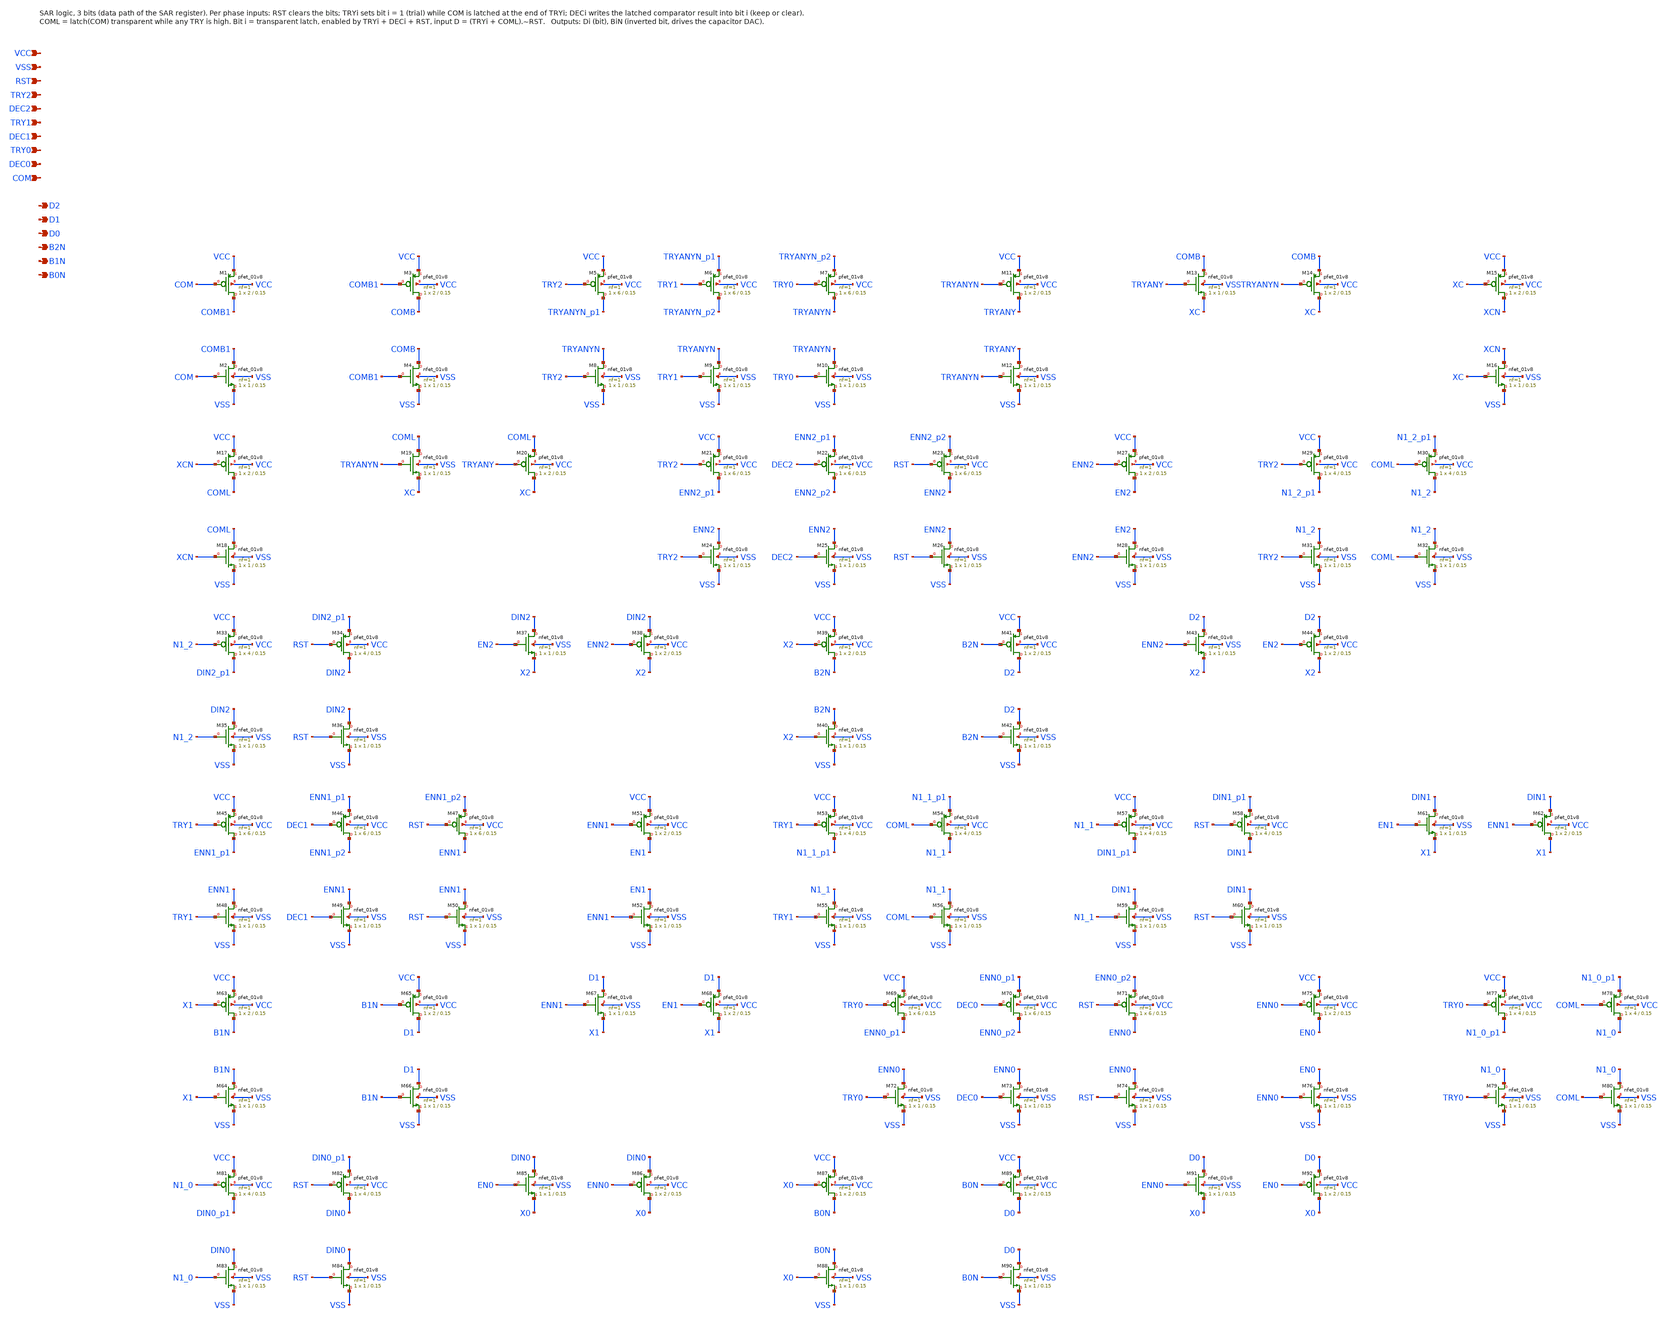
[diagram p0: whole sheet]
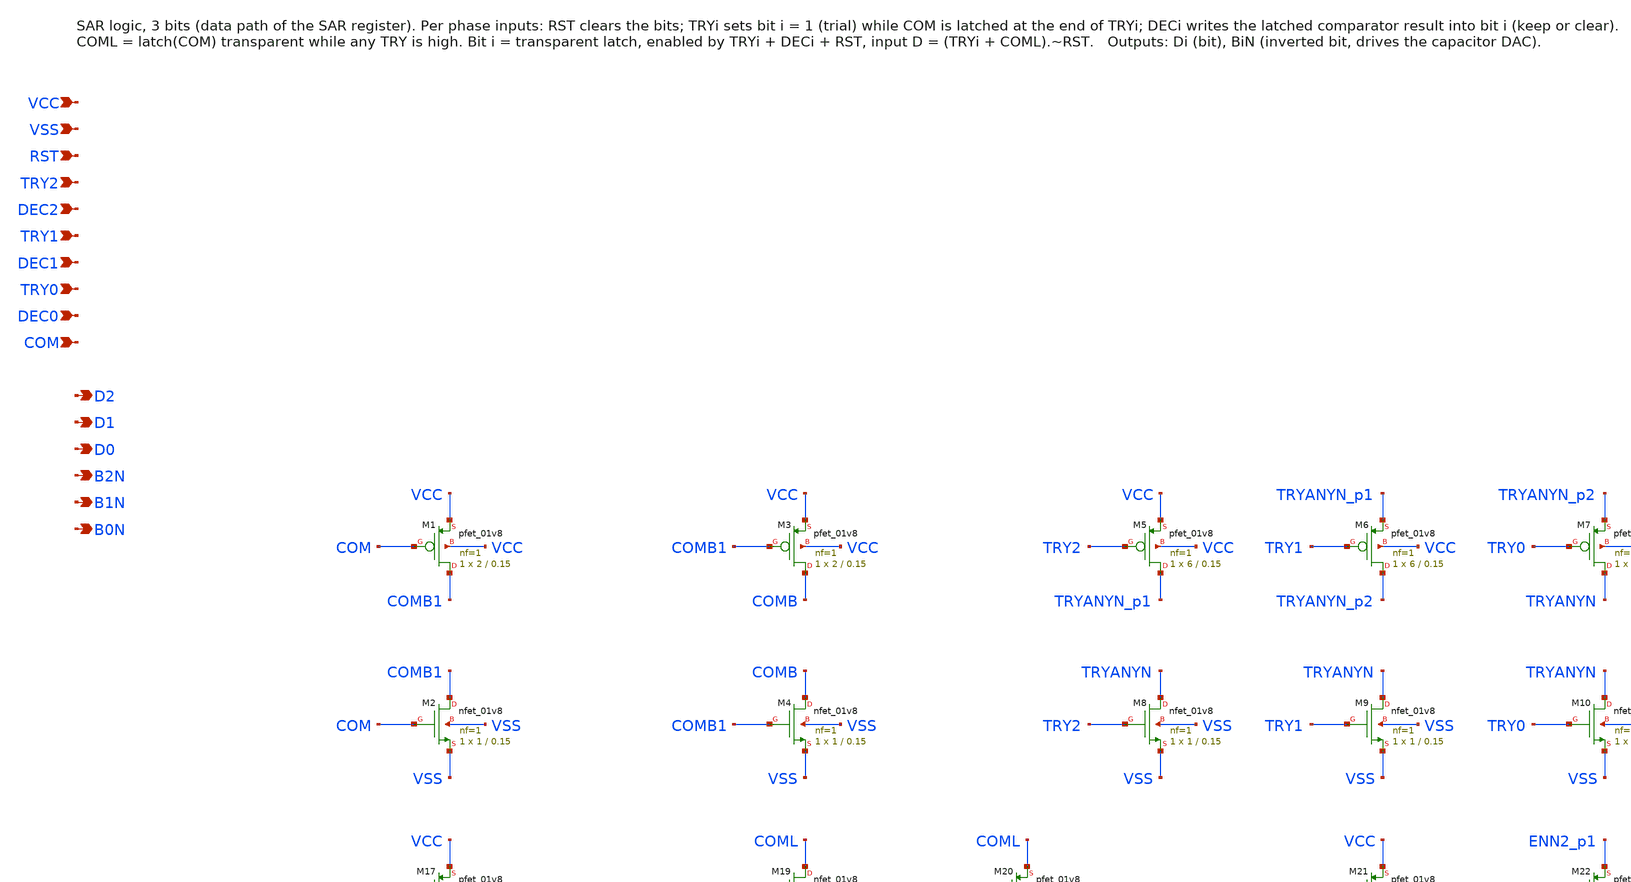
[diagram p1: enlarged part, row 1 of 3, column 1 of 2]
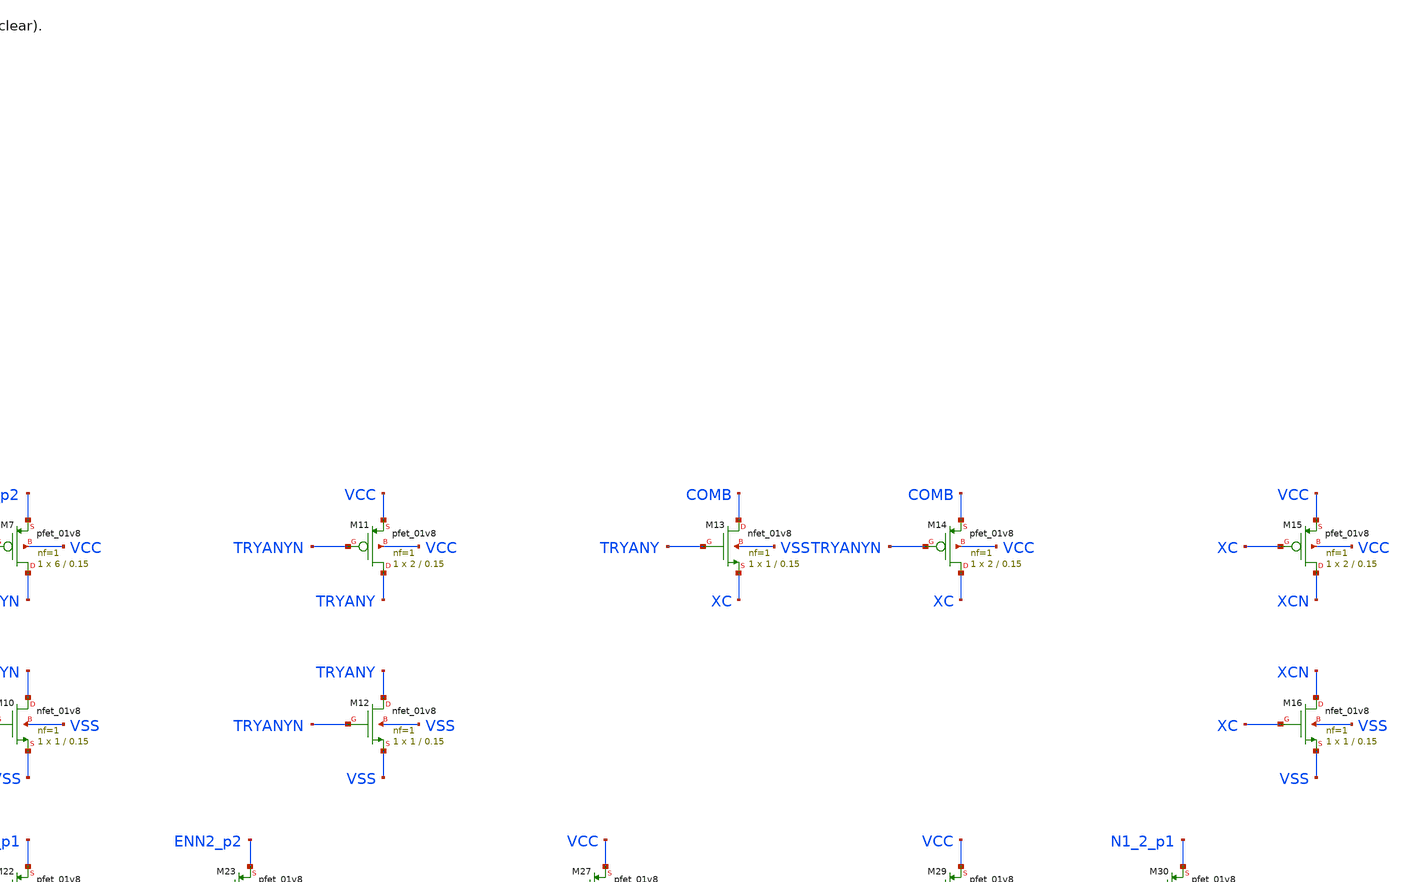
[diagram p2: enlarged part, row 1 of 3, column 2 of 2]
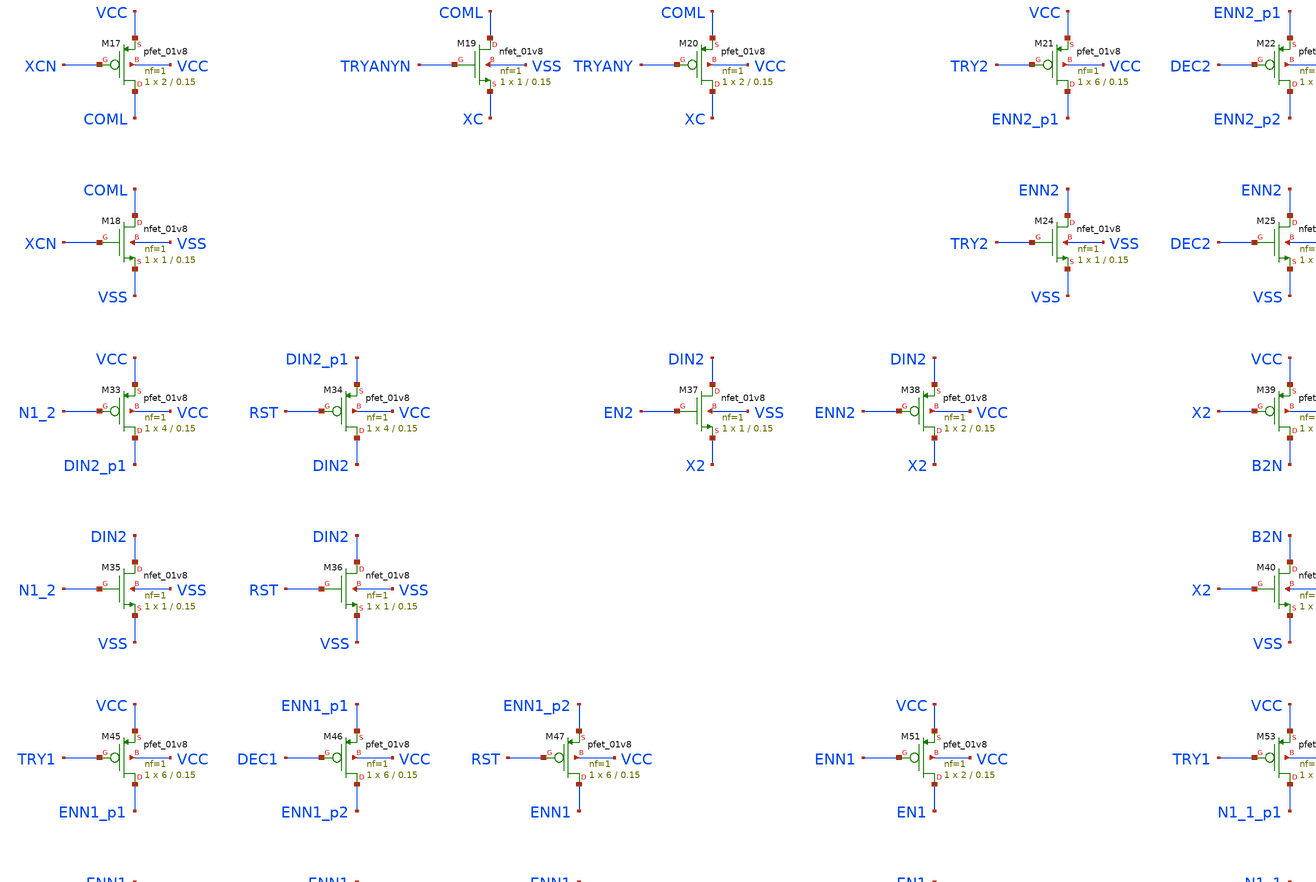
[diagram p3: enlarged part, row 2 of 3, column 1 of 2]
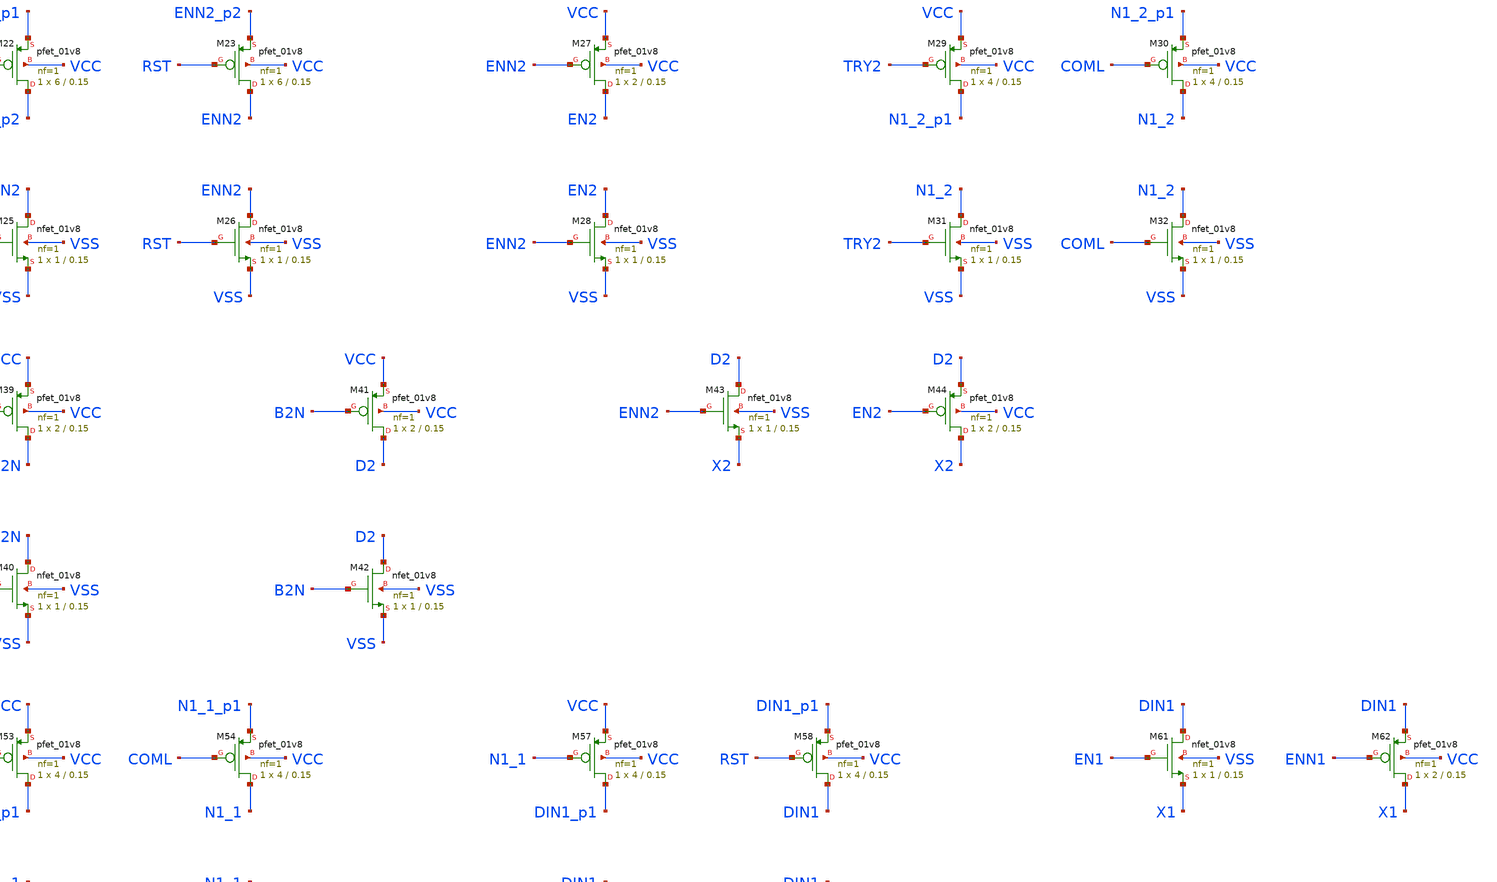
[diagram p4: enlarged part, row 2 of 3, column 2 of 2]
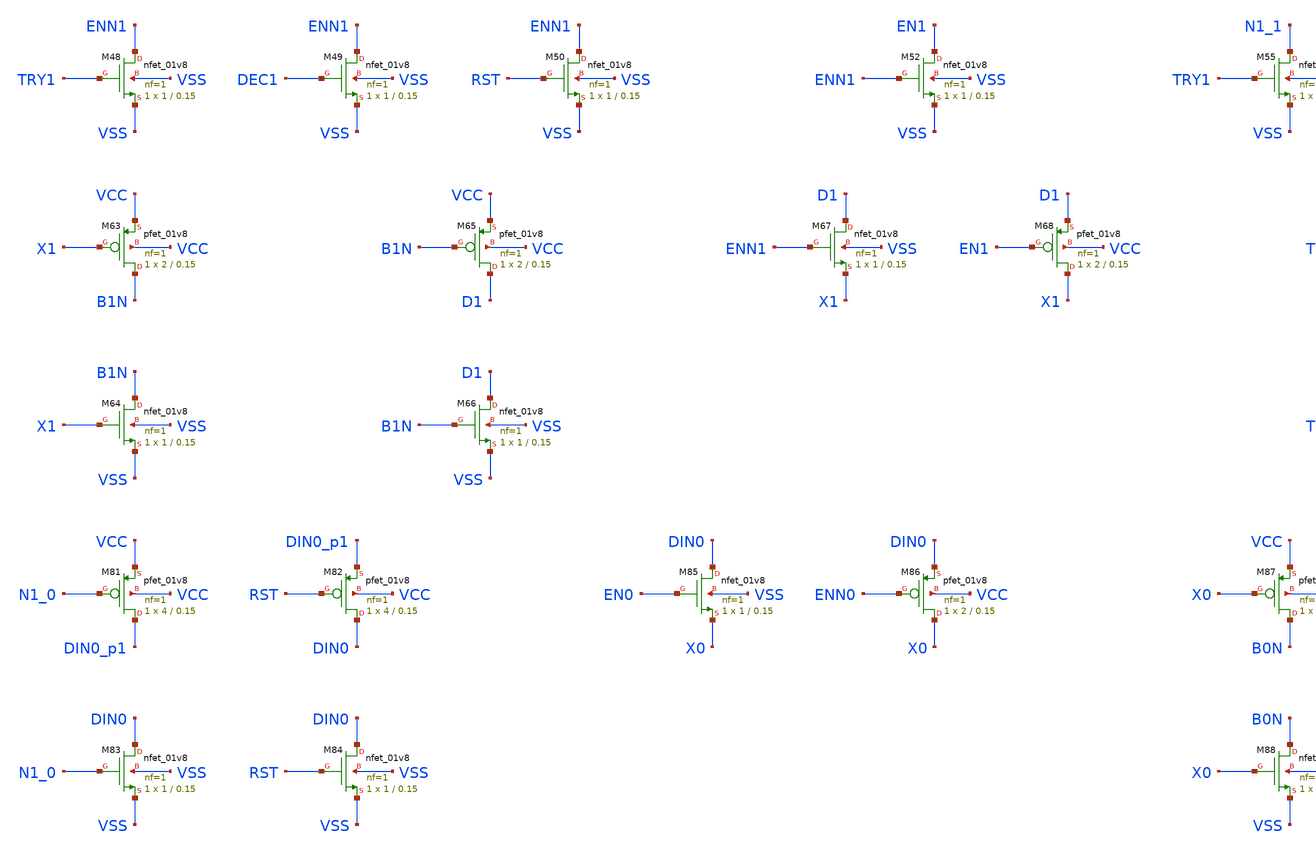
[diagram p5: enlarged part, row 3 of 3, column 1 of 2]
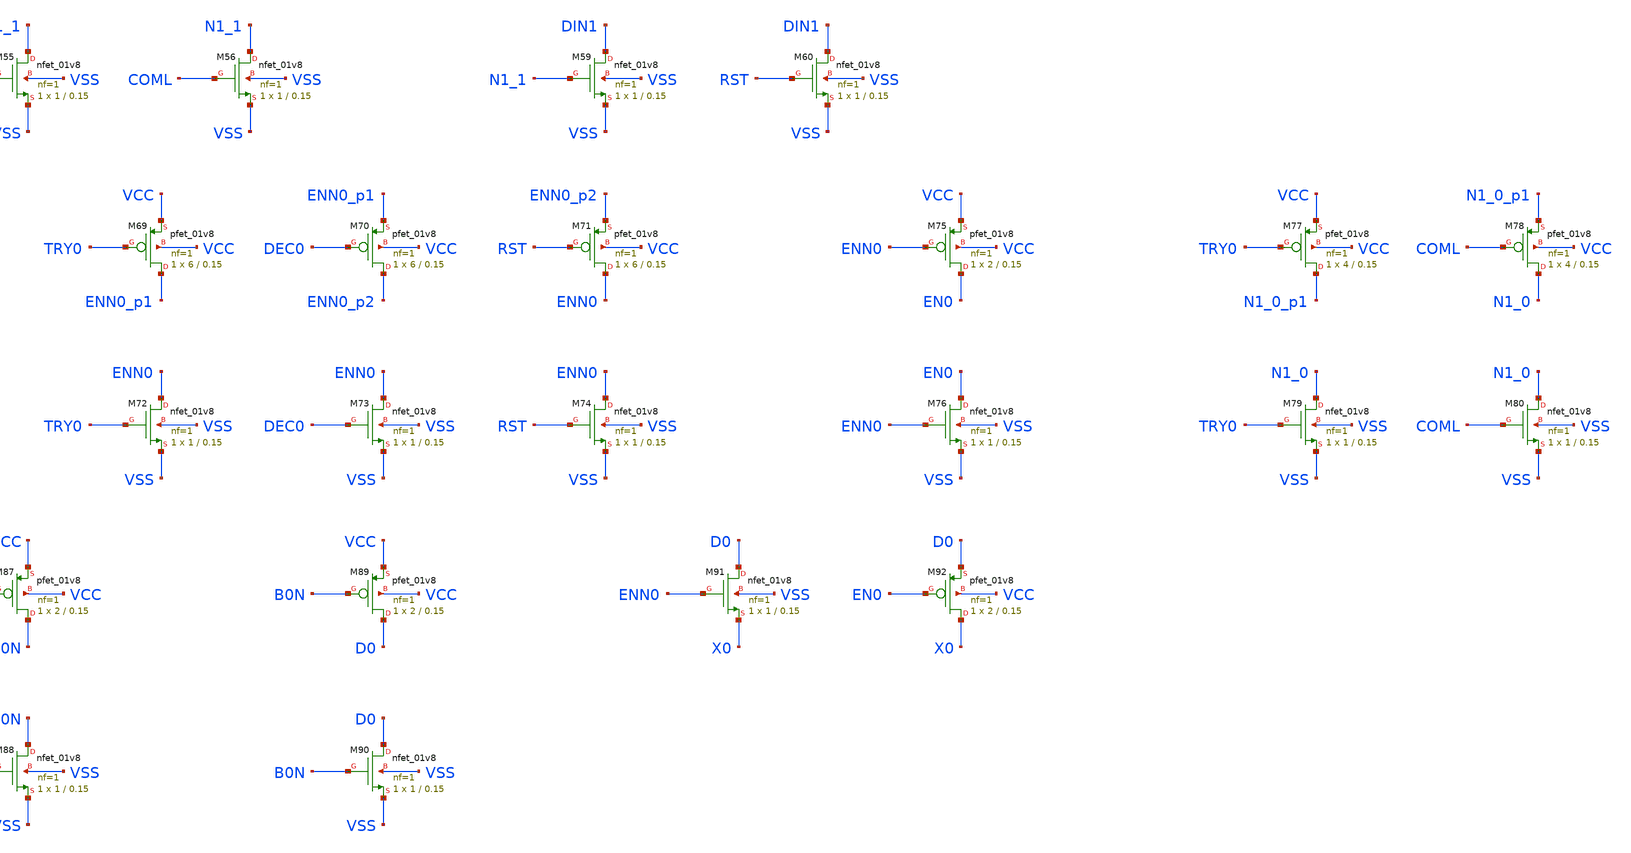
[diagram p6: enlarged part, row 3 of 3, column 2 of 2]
** sch_path: sar_logic3.sch
**.subckt sar_logic3 VCC VSS RST TRY2 DEC2 TRY1 DEC1 TRY0 DEC0 COM D2 D1 D0 B2N B1N B0N
*.ipin VCC
*.ipin VSS
*.ipin RST
*.ipin TRY2
*.ipin DEC2
*.ipin TRY1
*.ipin DEC1
*.ipin TRY0
*.ipin DEC0
*.ipin COM
*.opin D2
*.opin D1
*.opin D0
*.opin B2N
*.opin B1N
*.opin B0N
XM1 COMB1 COM VCC VCC sky130_fd_pr__pfet_01v8 L=0.15 W=2 nf=1 ad='int((nf+1)/2) * W/nf * 0.29' as='int((nf+2)/2) * W/nf * 0.29'
+ pd='2*int((nf+1)/2) * (W/nf + 0.29)' ps='2*int((nf+2)/2) * (W/nf + 0.29)' nrd='0.29 / W' nrs='0.29 / W'
+ sa=0 sb=0 sd=0 mult=1 m=1
XM2 COMB1 COM VSS VSS sky130_fd_pr__nfet_01v8 L=0.15 W=1 nf=1 ad='int((nf+1)/2) * W/nf * 0.29' as='int((nf+2)/2) * W/nf * 0.29'
+ pd='2*int((nf+1)/2) * (W/nf + 0.29)' ps='2*int((nf+2)/2) * (W/nf + 0.29)' nrd='0.29 / W' nrs='0.29 / W'
+ sa=0 sb=0 sd=0 mult=1 m=1
XM3 COMB COMB1 VCC VCC sky130_fd_pr__pfet_01v8 L=0.15 W=2 nf=1 ad='int((nf+1)/2) * W/nf * 0.29' as='int((nf+2)/2) * W/nf * 0.29'
+ pd='2*int((nf+1)/2) * (W/nf + 0.29)' ps='2*int((nf+2)/2) * (W/nf + 0.29)' nrd='0.29 / W' nrs='0.29 / W'
+ sa=0 sb=0 sd=0 mult=1 m=1
XM4 COMB COMB1 VSS VSS sky130_fd_pr__nfet_01v8 L=0.15 W=1 nf=1 ad='int((nf+1)/2) * W/nf * 0.29' as='int((nf+2)/2) * W/nf * 0.29'
+ pd='2*int((nf+1)/2) * (W/nf + 0.29)' ps='2*int((nf+2)/2) * (W/nf + 0.29)' nrd='0.29 / W' nrs='0.29 / W'
+ sa=0 sb=0 sd=0 mult=1 m=1
XM5 TRYANYN_p1 TRY2 VCC VCC sky130_fd_pr__pfet_01v8 L=0.15 W=6 nf=1 ad='int((nf+1)/2) * W/nf * 0.29'
+ as='int((nf+2)/2) * W/nf * 0.29' pd='2*int((nf+1)/2) * (W/nf + 0.29)' ps='2*int((nf+2)/2) * (W/nf + 0.29)'
+ nrd='0.29 / W' nrs='0.29 / W' sa=0 sb=0 sd=0 mult=1 m=1
XM6 TRYANYN_p2 TRY1 TRYANYN_p1 VCC sky130_fd_pr__pfet_01v8 L=0.15 W=6 nf=1 ad='int((nf+1)/2) * W/nf * 0.29'
+ as='int((nf+2)/2) * W/nf * 0.29' pd='2*int((nf+1)/2) * (W/nf + 0.29)' ps='2*int((nf+2)/2) * (W/nf + 0.29)'
+ nrd='0.29 / W' nrs='0.29 / W' sa=0 sb=0 sd=0 mult=1 m=1
XM7 TRYANYN TRY0 TRYANYN_p2 VCC sky130_fd_pr__pfet_01v8 L=0.15 W=6 nf=1 ad='int((nf+1)/2) * W/nf * 0.29'
+ as='int((nf+2)/2) * W/nf * 0.29' pd='2*int((nf+1)/2) * (W/nf + 0.29)' ps='2*int((nf+2)/2) * (W/nf + 0.29)'
+ nrd='0.29 / W' nrs='0.29 / W' sa=0 sb=0 sd=0 mult=1 m=1
XM8 TRYANYN TRY2 VSS VSS sky130_fd_pr__nfet_01v8 L=0.15 W=1 nf=1 ad='int((nf+1)/2) * W/nf * 0.29' as='int((nf+2)/2) * W/nf * 0.29'
+ pd='2*int((nf+1)/2) * (W/nf + 0.29)' ps='2*int((nf+2)/2) * (W/nf + 0.29)' nrd='0.29 / W' nrs='0.29 / W'
+ sa=0 sb=0 sd=0 mult=1 m=1
XM9 TRYANYN TRY1 VSS VSS sky130_fd_pr__nfet_01v8 L=0.15 W=1 nf=1 ad='int((nf+1)/2) * W/nf * 0.29' as='int((nf+2)/2) * W/nf * 0.29'
+ pd='2*int((nf+1)/2) * (W/nf + 0.29)' ps='2*int((nf+2)/2) * (W/nf + 0.29)' nrd='0.29 / W' nrs='0.29 / W'
+ sa=0 sb=0 sd=0 mult=1 m=1
XM10 TRYANYN TRY0 VSS VSS sky130_fd_pr__nfet_01v8 L=0.15 W=1 nf=1 ad='int((nf+1)/2) * W/nf * 0.29' as='int((nf+2)/2) * W/nf * 0.29'
+ pd='2*int((nf+1)/2) * (W/nf + 0.29)' ps='2*int((nf+2)/2) * (W/nf + 0.29)' nrd='0.29 / W' nrs='0.29 / W'
+ sa=0 sb=0 sd=0 mult=1 m=1
XM11 TRYANY TRYANYN VCC VCC sky130_fd_pr__pfet_01v8 L=0.15 W=2 nf=1 ad='int((nf+1)/2) * W/nf * 0.29'
+ as='int((nf+2)/2) * W/nf * 0.29' pd='2*int((nf+1)/2) * (W/nf + 0.29)' ps='2*int((nf+2)/2) * (W/nf + 0.29)'
+ nrd='0.29 / W' nrs='0.29 / W' sa=0 sb=0 sd=0 mult=1 m=1
XM12 TRYANY TRYANYN VSS VSS sky130_fd_pr__nfet_01v8 L=0.15 W=1 nf=1 ad='int((nf+1)/2) * W/nf * 0.29'
+ as='int((nf+2)/2) * W/nf * 0.29' pd='2*int((nf+1)/2) * (W/nf + 0.29)' ps='2*int((nf+2)/2) * (W/nf + 0.29)'
+ nrd='0.29 / W' nrs='0.29 / W' sa=0 sb=0 sd=0 mult=1 m=1
XM13 COMB TRYANY XC VSS sky130_fd_pr__nfet_01v8 L=0.15 W=1 nf=1 ad='int((nf+1)/2) * W/nf * 0.29' as='int((nf+2)/2) * W/nf * 0.29'
+ pd='2*int((nf+1)/2) * (W/nf + 0.29)' ps='2*int((nf+2)/2) * (W/nf + 0.29)' nrd='0.29 / W' nrs='0.29 / W'
+ sa=0 sb=0 sd=0 mult=1 m=1
XM14 XC TRYANYN COMB VCC sky130_fd_pr__pfet_01v8 L=0.15 W=2 nf=1 ad='int((nf+1)/2) * W/nf * 0.29' as='int((nf+2)/2) * W/nf * 0.29'
+ pd='2*int((nf+1)/2) * (W/nf + 0.29)' ps='2*int((nf+2)/2) * (W/nf + 0.29)' nrd='0.29 / W' nrs='0.29 / W'
+ sa=0 sb=0 sd=0 mult=1 m=1
XM15 XCN XC VCC VCC sky130_fd_pr__pfet_01v8 L=0.15 W=2 nf=1 ad='int((nf+1)/2) * W/nf * 0.29' as='int((nf+2)/2) * W/nf * 0.29'
+ pd='2*int((nf+1)/2) * (W/nf + 0.29)' ps='2*int((nf+2)/2) * (W/nf + 0.29)' nrd='0.29 / W' nrs='0.29 / W'
+ sa=0 sb=0 sd=0 mult=1 m=1
XM16 XCN XC VSS VSS sky130_fd_pr__nfet_01v8 L=0.15 W=1 nf=1 ad='int((nf+1)/2) * W/nf * 0.29' as='int((nf+2)/2) * W/nf * 0.29'
+ pd='2*int((nf+1)/2) * (W/nf + 0.29)' ps='2*int((nf+2)/2) * (W/nf + 0.29)' nrd='0.29 / W' nrs='0.29 / W'
+ sa=0 sb=0 sd=0 mult=1 m=1
XM17 COML XCN VCC VCC sky130_fd_pr__pfet_01v8 L=0.15 W=2 nf=1 ad='int((nf+1)/2) * W/nf * 0.29' as='int((nf+2)/2) * W/nf * 0.29'
+ pd='2*int((nf+1)/2) * (W/nf + 0.29)' ps='2*int((nf+2)/2) * (W/nf + 0.29)' nrd='0.29 / W' nrs='0.29 / W'
+ sa=0 sb=0 sd=0 mult=1 m=1
XM18 COML XCN VSS VSS sky130_fd_pr__nfet_01v8 L=0.15 W=1 nf=1 ad='int((nf+1)/2) * W/nf * 0.29' as='int((nf+2)/2) * W/nf * 0.29'
+ pd='2*int((nf+1)/2) * (W/nf + 0.29)' ps='2*int((nf+2)/2) * (W/nf + 0.29)' nrd='0.29 / W' nrs='0.29 / W'
+ sa=0 sb=0 sd=0 mult=1 m=1
XM19 COML TRYANYN XC VSS sky130_fd_pr__nfet_01v8 L=0.15 W=1 nf=1 ad='int((nf+1)/2) * W/nf * 0.29' as='int((nf+2)/2) * W/nf * 0.29'
+ pd='2*int((nf+1)/2) * (W/nf + 0.29)' ps='2*int((nf+2)/2) * (W/nf + 0.29)' nrd='0.29 / W' nrs='0.29 / W'
+ sa=0 sb=0 sd=0 mult=1 m=1
XM20 XC TRYANY COML VCC sky130_fd_pr__pfet_01v8 L=0.15 W=2 nf=1 ad='int((nf+1)/2) * W/nf * 0.29' as='int((nf+2)/2) * W/nf * 0.29'
+ pd='2*int((nf+1)/2) * (W/nf + 0.29)' ps='2*int((nf+2)/2) * (W/nf + 0.29)' nrd='0.29 / W' nrs='0.29 / W'
+ sa=0 sb=0 sd=0 mult=1 m=1
XM21 ENN2_p1 TRY2 VCC VCC sky130_fd_pr__pfet_01v8 L=0.15 W=6 nf=1 ad='int((nf+1)/2) * W/nf * 0.29' as='int((nf+2)/2) * W/nf * 0.29'
+ pd='2*int((nf+1)/2) * (W/nf + 0.29)' ps='2*int((nf+2)/2) * (W/nf + 0.29)' nrd='0.29 / W' nrs='0.29 / W'
+ sa=0 sb=0 sd=0 mult=1 m=1
XM22 ENN2_p2 DEC2 ENN2_p1 VCC sky130_fd_pr__pfet_01v8 L=0.15 W=6 nf=1 ad='int((nf+1)/2) * W/nf * 0.29'
+ as='int((nf+2)/2) * W/nf * 0.29' pd='2*int((nf+1)/2) * (W/nf + 0.29)' ps='2*int((nf+2)/2) * (W/nf + 0.29)'
+ nrd='0.29 / W' nrs='0.29 / W' sa=0 sb=0 sd=0 mult=1 m=1
XM23 ENN2 RST ENN2_p2 VCC sky130_fd_pr__pfet_01v8 L=0.15 W=6 nf=1 ad='int((nf+1)/2) * W/nf * 0.29' as='int((nf+2)/2) * W/nf * 0.29'
+ pd='2*int((nf+1)/2) * (W/nf + 0.29)' ps='2*int((nf+2)/2) * (W/nf + 0.29)' nrd='0.29 / W' nrs='0.29 / W'
+ sa=0 sb=0 sd=0 mult=1 m=1
XM24 ENN2 TRY2 VSS VSS sky130_fd_pr__nfet_01v8 L=0.15 W=1 nf=1 ad='int((nf+1)/2) * W/nf * 0.29' as='int((nf+2)/2) * W/nf * 0.29'
+ pd='2*int((nf+1)/2) * (W/nf + 0.29)' ps='2*int((nf+2)/2) * (W/nf + 0.29)' nrd='0.29 / W' nrs='0.29 / W'
+ sa=0 sb=0 sd=0 mult=1 m=1
XM25 ENN2 DEC2 VSS VSS sky130_fd_pr__nfet_01v8 L=0.15 W=1 nf=1 ad='int((nf+1)/2) * W/nf * 0.29' as='int((nf+2)/2) * W/nf * 0.29'
+ pd='2*int((nf+1)/2) * (W/nf + 0.29)' ps='2*int((nf+2)/2) * (W/nf + 0.29)' nrd='0.29 / W' nrs='0.29 / W'
+ sa=0 sb=0 sd=0 mult=1 m=1
XM26 ENN2 RST VSS VSS sky130_fd_pr__nfet_01v8 L=0.15 W=1 nf=1 ad='int((nf+1)/2) * W/nf * 0.29' as='int((nf+2)/2) * W/nf * 0.29'
+ pd='2*int((nf+1)/2) * (W/nf + 0.29)' ps='2*int((nf+2)/2) * (W/nf + 0.29)' nrd='0.29 / W' nrs='0.29 / W'
+ sa=0 sb=0 sd=0 mult=1 m=1
XM27 EN2 ENN2 VCC VCC sky130_fd_pr__pfet_01v8 L=0.15 W=2 nf=1 ad='int((nf+1)/2) * W/nf * 0.29' as='int((nf+2)/2) * W/nf * 0.29'
+ pd='2*int((nf+1)/2) * (W/nf + 0.29)' ps='2*int((nf+2)/2) * (W/nf + 0.29)' nrd='0.29 / W' nrs='0.29 / W'
+ sa=0 sb=0 sd=0 mult=1 m=1
XM28 EN2 ENN2 VSS VSS sky130_fd_pr__nfet_01v8 L=0.15 W=1 nf=1 ad='int((nf+1)/2) * W/nf * 0.29' as='int((nf+2)/2) * W/nf * 0.29'
+ pd='2*int((nf+1)/2) * (W/nf + 0.29)' ps='2*int((nf+2)/2) * (W/nf + 0.29)' nrd='0.29 / W' nrs='0.29 / W'
+ sa=0 sb=0 sd=0 mult=1 m=1
XM29 N1_2_p1 TRY2 VCC VCC sky130_fd_pr__pfet_01v8 L=0.15 W=4 nf=1 ad='int((nf+1)/2) * W/nf * 0.29' as='int((nf+2)/2) * W/nf * 0.29'
+ pd='2*int((nf+1)/2) * (W/nf + 0.29)' ps='2*int((nf+2)/2) * (W/nf + 0.29)' nrd='0.29 / W' nrs='0.29 / W'
+ sa=0 sb=0 sd=0 mult=1 m=1
XM30 N1_2 COML N1_2_p1 VCC sky130_fd_pr__pfet_01v8 L=0.15 W=4 nf=1 ad='int((nf+1)/2) * W/nf * 0.29' as='int((nf+2)/2) * W/nf * 0.29'
+ pd='2*int((nf+1)/2) * (W/nf + 0.29)' ps='2*int((nf+2)/2) * (W/nf + 0.29)' nrd='0.29 / W' nrs='0.29 / W'
+ sa=0 sb=0 sd=0 mult=1 m=1
XM31 N1_2 TRY2 VSS VSS sky130_fd_pr__nfet_01v8 L=0.15 W=1 nf=1 ad='int((nf+1)/2) * W/nf * 0.29' as='int((nf+2)/2) * W/nf * 0.29'
+ pd='2*int((nf+1)/2) * (W/nf + 0.29)' ps='2*int((nf+2)/2) * (W/nf + 0.29)' nrd='0.29 / W' nrs='0.29 / W'
+ sa=0 sb=0 sd=0 mult=1 m=1
XM32 N1_2 COML VSS VSS sky130_fd_pr__nfet_01v8 L=0.15 W=1 nf=1 ad='int((nf+1)/2) * W/nf * 0.29' as='int((nf+2)/2) * W/nf * 0.29'
+ pd='2*int((nf+1)/2) * (W/nf + 0.29)' ps='2*int((nf+2)/2) * (W/nf + 0.29)' nrd='0.29 / W' nrs='0.29 / W'
+ sa=0 sb=0 sd=0 mult=1 m=1
XM33 DIN2_p1 N1_2 VCC VCC sky130_fd_pr__pfet_01v8 L=0.15 W=4 nf=1 ad='int((nf+1)/2) * W/nf * 0.29' as='int((nf+2)/2) * W/nf * 0.29'
+ pd='2*int((nf+1)/2) * (W/nf + 0.29)' ps='2*int((nf+2)/2) * (W/nf + 0.29)' nrd='0.29 / W' nrs='0.29 / W'
+ sa=0 sb=0 sd=0 mult=1 m=1
XM34 DIN2 RST DIN2_p1 VCC sky130_fd_pr__pfet_01v8 L=0.15 W=4 nf=1 ad='int((nf+1)/2) * W/nf * 0.29' as='int((nf+2)/2) * W/nf * 0.29'
+ pd='2*int((nf+1)/2) * (W/nf + 0.29)' ps='2*int((nf+2)/2) * (W/nf + 0.29)' nrd='0.29 / W' nrs='0.29 / W'
+ sa=0 sb=0 sd=0 mult=1 m=1
XM35 DIN2 N1_2 VSS VSS sky130_fd_pr__nfet_01v8 L=0.15 W=1 nf=1 ad='int((nf+1)/2) * W/nf * 0.29' as='int((nf+2)/2) * W/nf * 0.29'
+ pd='2*int((nf+1)/2) * (W/nf + 0.29)' ps='2*int((nf+2)/2) * (W/nf + 0.29)' nrd='0.29 / W' nrs='0.29 / W'
+ sa=0 sb=0 sd=0 mult=1 m=1
XM36 DIN2 RST VSS VSS sky130_fd_pr__nfet_01v8 L=0.15 W=1 nf=1 ad='int((nf+1)/2) * W/nf * 0.29' as='int((nf+2)/2) * W/nf * 0.29'
+ pd='2*int((nf+1)/2) * (W/nf + 0.29)' ps='2*int((nf+2)/2) * (W/nf + 0.29)' nrd='0.29 / W' nrs='0.29 / W'
+ sa=0 sb=0 sd=0 mult=1 m=1
XM37 DIN2 EN2 X2 VSS sky130_fd_pr__nfet_01v8 L=0.15 W=1 nf=1 ad='int((nf+1)/2) * W/nf * 0.29' as='int((nf+2)/2) * W/nf * 0.29'
+ pd='2*int((nf+1)/2) * (W/nf + 0.29)' ps='2*int((nf+2)/2) * (W/nf + 0.29)' nrd='0.29 / W' nrs='0.29 / W'
+ sa=0 sb=0 sd=0 mult=1 m=1
XM38 X2 ENN2 DIN2 VCC sky130_fd_pr__pfet_01v8 L=0.15 W=2 nf=1 ad='int((nf+1)/2) * W/nf * 0.29' as='int((nf+2)/2) * W/nf * 0.29'
+ pd='2*int((nf+1)/2) * (W/nf + 0.29)' ps='2*int((nf+2)/2) * (W/nf + 0.29)' nrd='0.29 / W' nrs='0.29 / W'
+ sa=0 sb=0 sd=0 mult=1 m=1
XM39 B2N X2 VCC VCC sky130_fd_pr__pfet_01v8 L=0.15 W=2 nf=1 ad='int((nf+1)/2) * W/nf * 0.29' as='int((nf+2)/2) * W/nf * 0.29'
+ pd='2*int((nf+1)/2) * (W/nf + 0.29)' ps='2*int((nf+2)/2) * (W/nf + 0.29)' nrd='0.29 / W' nrs='0.29 / W'
+ sa=0 sb=0 sd=0 mult=1 m=1
XM40 B2N X2 VSS VSS sky130_fd_pr__nfet_01v8 L=0.15 W=1 nf=1 ad='int((nf+1)/2) * W/nf * 0.29' as='int((nf+2)/2) * W/nf * 0.29'
+ pd='2*int((nf+1)/2) * (W/nf + 0.29)' ps='2*int((nf+2)/2) * (W/nf + 0.29)' nrd='0.29 / W' nrs='0.29 / W'
+ sa=0 sb=0 sd=0 mult=1 m=1
XM41 D2 B2N VCC VCC sky130_fd_pr__pfet_01v8 L=0.15 W=2 nf=1 ad='int((nf+1)/2) * W/nf * 0.29' as='int((nf+2)/2) * W/nf * 0.29'
+ pd='2*int((nf+1)/2) * (W/nf + 0.29)' ps='2*int((nf+2)/2) * (W/nf + 0.29)' nrd='0.29 / W' nrs='0.29 / W'
+ sa=0 sb=0 sd=0 mult=1 m=1
XM42 D2 B2N VSS VSS sky130_fd_pr__nfet_01v8 L=0.15 W=1 nf=1 ad='int((nf+1)/2) * W/nf * 0.29' as='int((nf+2)/2) * W/nf * 0.29'
+ pd='2*int((nf+1)/2) * (W/nf + 0.29)' ps='2*int((nf+2)/2) * (W/nf + 0.29)' nrd='0.29 / W' nrs='0.29 / W'
+ sa=0 sb=0 sd=0 mult=1 m=1
XM43 D2 ENN2 X2 VSS sky130_fd_pr__nfet_01v8 L=0.15 W=1 nf=1 ad='int((nf+1)/2) * W/nf * 0.29' as='int((nf+2)/2) * W/nf * 0.29'
+ pd='2*int((nf+1)/2) * (W/nf + 0.29)' ps='2*int((nf+2)/2) * (W/nf + 0.29)' nrd='0.29 / W' nrs='0.29 / W'
+ sa=0 sb=0 sd=0 mult=1 m=1
XM44 X2 EN2 D2 VCC sky130_fd_pr__pfet_01v8 L=0.15 W=2 nf=1 ad='int((nf+1)/2) * W/nf * 0.29' as='int((nf+2)/2) * W/nf * 0.29'
+ pd='2*int((nf+1)/2) * (W/nf + 0.29)' ps='2*int((nf+2)/2) * (W/nf + 0.29)' nrd='0.29 / W' nrs='0.29 / W'
+ sa=0 sb=0 sd=0 mult=1 m=1
XM45 ENN1_p1 TRY1 VCC VCC sky130_fd_pr__pfet_01v8 L=0.15 W=6 nf=1 ad='int((nf+1)/2) * W/nf * 0.29' as='int((nf+2)/2) * W/nf * 0.29'
+ pd='2*int((nf+1)/2) * (W/nf + 0.29)' ps='2*int((nf+2)/2) * (W/nf + 0.29)' nrd='0.29 / W' nrs='0.29 / W'
+ sa=0 sb=0 sd=0 mult=1 m=1
XM46 ENN1_p2 DEC1 ENN1_p1 VCC sky130_fd_pr__pfet_01v8 L=0.15 W=6 nf=1 ad='int((nf+1)/2) * W/nf * 0.29'
+ as='int((nf+2)/2) * W/nf * 0.29' pd='2*int((nf+1)/2) * (W/nf + 0.29)' ps='2*int((nf+2)/2) * (W/nf + 0.29)'
+ nrd='0.29 / W' nrs='0.29 / W' sa=0 sb=0 sd=0 mult=1 m=1
XM47 ENN1 RST ENN1_p2 VCC sky130_fd_pr__pfet_01v8 L=0.15 W=6 nf=1 ad='int((nf+1)/2) * W/nf * 0.29' as='int((nf+2)/2) * W/nf * 0.29'
+ pd='2*int((nf+1)/2) * (W/nf + 0.29)' ps='2*int((nf+2)/2) * (W/nf + 0.29)' nrd='0.29 / W' nrs='0.29 / W'
+ sa=0 sb=0 sd=0 mult=1 m=1
XM48 ENN1 TRY1 VSS VSS sky130_fd_pr__nfet_01v8 L=0.15 W=1 nf=1 ad='int((nf+1)/2) * W/nf * 0.29' as='int((nf+2)/2) * W/nf * 0.29'
+ pd='2*int((nf+1)/2) * (W/nf + 0.29)' ps='2*int((nf+2)/2) * (W/nf + 0.29)' nrd='0.29 / W' nrs='0.29 / W'
+ sa=0 sb=0 sd=0 mult=1 m=1
XM49 ENN1 DEC1 VSS VSS sky130_fd_pr__nfet_01v8 L=0.15 W=1 nf=1 ad='int((nf+1)/2) * W/nf * 0.29' as='int((nf+2)/2) * W/nf * 0.29'
+ pd='2*int((nf+1)/2) * (W/nf + 0.29)' ps='2*int((nf+2)/2) * (W/nf + 0.29)' nrd='0.29 / W' nrs='0.29 / W'
+ sa=0 sb=0 sd=0 mult=1 m=1
XM50 ENN1 RST VSS VSS sky130_fd_pr__nfet_01v8 L=0.15 W=1 nf=1 ad='int((nf+1)/2) * W/nf * 0.29' as='int((nf+2)/2) * W/nf * 0.29'
+ pd='2*int((nf+1)/2) * (W/nf + 0.29)' ps='2*int((nf+2)/2) * (W/nf + 0.29)' nrd='0.29 / W' nrs='0.29 / W'
+ sa=0 sb=0 sd=0 mult=1 m=1
XM51 EN1 ENN1 VCC VCC sky130_fd_pr__pfet_01v8 L=0.15 W=2 nf=1 ad='int((nf+1)/2) * W/nf * 0.29' as='int((nf+2)/2) * W/nf * 0.29'
+ pd='2*int((nf+1)/2) * (W/nf + 0.29)' ps='2*int((nf+2)/2) * (W/nf + 0.29)' nrd='0.29 / W' nrs='0.29 / W'
+ sa=0 sb=0 sd=0 mult=1 m=1
XM52 EN1 ENN1 VSS VSS sky130_fd_pr__nfet_01v8 L=0.15 W=1 nf=1 ad='int((nf+1)/2) * W/nf * 0.29' as='int((nf+2)/2) * W/nf * 0.29'
+ pd='2*int((nf+1)/2) * (W/nf + 0.29)' ps='2*int((nf+2)/2) * (W/nf + 0.29)' nrd='0.29 / W' nrs='0.29 / W'
+ sa=0 sb=0 sd=0 mult=1 m=1
XM53 N1_1_p1 TRY1 VCC VCC sky130_fd_pr__pfet_01v8 L=0.15 W=4 nf=1 ad='int((nf+1)/2) * W/nf * 0.29' as='int((nf+2)/2) * W/nf * 0.29'
+ pd='2*int((nf+1)/2) * (W/nf + 0.29)' ps='2*int((nf+2)/2) * (W/nf + 0.29)' nrd='0.29 / W' nrs='0.29 / W'
+ sa=0 sb=0 sd=0 mult=1 m=1
XM54 N1_1 COML N1_1_p1 VCC sky130_fd_pr__pfet_01v8 L=0.15 W=4 nf=1 ad='int((nf+1)/2) * W/nf * 0.29' as='int((nf+2)/2) * W/nf * 0.29'
+ pd='2*int((nf+1)/2) * (W/nf + 0.29)' ps='2*int((nf+2)/2) * (W/nf + 0.29)' nrd='0.29 / W' nrs='0.29 / W'
+ sa=0 sb=0 sd=0 mult=1 m=1
XM55 N1_1 TRY1 VSS VSS sky130_fd_pr__nfet_01v8 L=0.15 W=1 nf=1 ad='int((nf+1)/2) * W/nf * 0.29' as='int((nf+2)/2) * W/nf * 0.29'
+ pd='2*int((nf+1)/2) * (W/nf + 0.29)' ps='2*int((nf+2)/2) * (W/nf + 0.29)' nrd='0.29 / W' nrs='0.29 / W'
+ sa=0 sb=0 sd=0 mult=1 m=1
XM56 N1_1 COML VSS VSS sky130_fd_pr__nfet_01v8 L=0.15 W=1 nf=1 ad='int((nf+1)/2) * W/nf * 0.29' as='int((nf+2)/2) * W/nf * 0.29'
+ pd='2*int((nf+1)/2) * (W/nf + 0.29)' ps='2*int((nf+2)/2) * (W/nf + 0.29)' nrd='0.29 / W' nrs='0.29 / W'
+ sa=0 sb=0 sd=0 mult=1 m=1
XM57 DIN1_p1 N1_1 VCC VCC sky130_fd_pr__pfet_01v8 L=0.15 W=4 nf=1 ad='int((nf+1)/2) * W/nf * 0.29' as='int((nf+2)/2) * W/nf * 0.29'
+ pd='2*int((nf+1)/2) * (W/nf + 0.29)' ps='2*int((nf+2)/2) * (W/nf + 0.29)' nrd='0.29 / W' nrs='0.29 / W'
+ sa=0 sb=0 sd=0 mult=1 m=1
XM58 DIN1 RST DIN1_p1 VCC sky130_fd_pr__pfet_01v8 L=0.15 W=4 nf=1 ad='int((nf+1)/2) * W/nf * 0.29' as='int((nf+2)/2) * W/nf * 0.29'
+ pd='2*int((nf+1)/2) * (W/nf + 0.29)' ps='2*int((nf+2)/2) * (W/nf + 0.29)' nrd='0.29 / W' nrs='0.29 / W'
+ sa=0 sb=0 sd=0 mult=1 m=1
XM59 DIN1 N1_1 VSS VSS sky130_fd_pr__nfet_01v8 L=0.15 W=1 nf=1 ad='int((nf+1)/2) * W/nf * 0.29' as='int((nf+2)/2) * W/nf * 0.29'
+ pd='2*int((nf+1)/2) * (W/nf + 0.29)' ps='2*int((nf+2)/2) * (W/nf + 0.29)' nrd='0.29 / W' nrs='0.29 / W'
+ sa=0 sb=0 sd=0 mult=1 m=1
XM60 DIN1 RST VSS VSS sky130_fd_pr__nfet_01v8 L=0.15 W=1 nf=1 ad='int((nf+1)/2) * W/nf * 0.29' as='int((nf+2)/2) * W/nf * 0.29'
+ pd='2*int((nf+1)/2) * (W/nf + 0.29)' ps='2*int((nf+2)/2) * (W/nf + 0.29)' nrd='0.29 / W' nrs='0.29 / W'
+ sa=0 sb=0 sd=0 mult=1 m=1
XM61 DIN1 EN1 X1 VSS sky130_fd_pr__nfet_01v8 L=0.15 W=1 nf=1 ad='int((nf+1)/2) * W/nf * 0.29' as='int((nf+2)/2) * W/nf * 0.29'
+ pd='2*int((nf+1)/2) * (W/nf + 0.29)' ps='2*int((nf+2)/2) * (W/nf + 0.29)' nrd='0.29 / W' nrs='0.29 / W'
+ sa=0 sb=0 sd=0 mult=1 m=1
XM62 X1 ENN1 DIN1 VCC sky130_fd_pr__pfet_01v8 L=0.15 W=2 nf=1 ad='int((nf+1)/2) * W/nf * 0.29' as='int((nf+2)/2) * W/nf * 0.29'
+ pd='2*int((nf+1)/2) * (W/nf + 0.29)' ps='2*int((nf+2)/2) * (W/nf + 0.29)' nrd='0.29 / W' nrs='0.29 / W'
+ sa=0 sb=0 sd=0 mult=1 m=1
XM63 B1N X1 VCC VCC sky130_fd_pr__pfet_01v8 L=0.15 W=2 nf=1 ad='int((nf+1)/2) * W/nf * 0.29' as='int((nf+2)/2) * W/nf * 0.29'
+ pd='2*int((nf+1)/2) * (W/nf + 0.29)' ps='2*int((nf+2)/2) * (W/nf + 0.29)' nrd='0.29 / W' nrs='0.29 / W'
+ sa=0 sb=0 sd=0 mult=1 m=1
XM64 B1N X1 VSS VSS sky130_fd_pr__nfet_01v8 L=0.15 W=1 nf=1 ad='int((nf+1)/2) * W/nf * 0.29' as='int((nf+2)/2) * W/nf * 0.29'
+ pd='2*int((nf+1)/2) * (W/nf + 0.29)' ps='2*int((nf+2)/2) * (W/nf + 0.29)' nrd='0.29 / W' nrs='0.29 / W'
+ sa=0 sb=0 sd=0 mult=1 m=1
XM65 D1 B1N VCC VCC sky130_fd_pr__pfet_01v8 L=0.15 W=2 nf=1 ad='int((nf+1)/2) * W/nf * 0.29' as='int((nf+2)/2) * W/nf * 0.29'
+ pd='2*int((nf+1)/2) * (W/nf + 0.29)' ps='2*int((nf+2)/2) * (W/nf + 0.29)' nrd='0.29 / W' nrs='0.29 / W'
+ sa=0 sb=0 sd=0 mult=1 m=1
XM66 D1 B1N VSS VSS sky130_fd_pr__nfet_01v8 L=0.15 W=1 nf=1 ad='int((nf+1)/2) * W/nf * 0.29' as='int((nf+2)/2) * W/nf * 0.29'
+ pd='2*int((nf+1)/2) * (W/nf + 0.29)' ps='2*int((nf+2)/2) * (W/nf + 0.29)' nrd='0.29 / W' nrs='0.29 / W'
+ sa=0 sb=0 sd=0 mult=1 m=1
XM67 D1 ENN1 X1 VSS sky130_fd_pr__nfet_01v8 L=0.15 W=1 nf=1 ad='int((nf+1)/2) * W/nf * 0.29' as='int((nf+2)/2) * W/nf * 0.29'
+ pd='2*int((nf+1)/2) * (W/nf + 0.29)' ps='2*int((nf+2)/2) * (W/nf + 0.29)' nrd='0.29 / W' nrs='0.29 / W'
+ sa=0 sb=0 sd=0 mult=1 m=1
XM68 X1 EN1 D1 VCC sky130_fd_pr__pfet_01v8 L=0.15 W=2 nf=1 ad='int((nf+1)/2) * W/nf * 0.29' as='int((nf+2)/2) * W/nf * 0.29'
+ pd='2*int((nf+1)/2) * (W/nf + 0.29)' ps='2*int((nf+2)/2) * (W/nf + 0.29)' nrd='0.29 / W' nrs='0.29 / W'
+ sa=0 sb=0 sd=0 mult=1 m=1
XM69 ENN0_p1 TRY0 VCC VCC sky130_fd_pr__pfet_01v8 L=0.15 W=6 nf=1 ad='int((nf+1)/2) * W/nf * 0.29' as='int((nf+2)/2) * W/nf * 0.29'
+ pd='2*int((nf+1)/2) * (W/nf + 0.29)' ps='2*int((nf+2)/2) * (W/nf + 0.29)' nrd='0.29 / W' nrs='0.29 / W'
+ sa=0 sb=0 sd=0 mult=1 m=1
XM70 ENN0_p2 DEC0 ENN0_p1 VCC sky130_fd_pr__pfet_01v8 L=0.15 W=6 nf=1 ad='int((nf+1)/2) * W/nf * 0.29'
+ as='int((nf+2)/2) * W/nf * 0.29' pd='2*int((nf+1)/2) * (W/nf + 0.29)' ps='2*int((nf+2)/2) * (W/nf + 0.29)'
+ nrd='0.29 / W' nrs='0.29 / W' sa=0 sb=0 sd=0 mult=1 m=1
XM71 ENN0 RST ENN0_p2 VCC sky130_fd_pr__pfet_01v8 L=0.15 W=6 nf=1 ad='int((nf+1)/2) * W/nf * 0.29' as='int((nf+2)/2) * W/nf * 0.29'
+ pd='2*int((nf+1)/2) * (W/nf + 0.29)' ps='2*int((nf+2)/2) * (W/nf + 0.29)' nrd='0.29 / W' nrs='0.29 / W'
+ sa=0 sb=0 sd=0 mult=1 m=1
XM72 ENN0 TRY0 VSS VSS sky130_fd_pr__nfet_01v8 L=0.15 W=1 nf=1 ad='int((nf+1)/2) * W/nf * 0.29' as='int((nf+2)/2) * W/nf * 0.29'
+ pd='2*int((nf+1)/2) * (W/nf + 0.29)' ps='2*int((nf+2)/2) * (W/nf + 0.29)' nrd='0.29 / W' nrs='0.29 / W'
+ sa=0 sb=0 sd=0 mult=1 m=1
XM73 ENN0 DEC0 VSS VSS sky130_fd_pr__nfet_01v8 L=0.15 W=1 nf=1 ad='int((nf+1)/2) * W/nf * 0.29' as='int((nf+2)/2) * W/nf * 0.29'
+ pd='2*int((nf+1)/2) * (W/nf + 0.29)' ps='2*int((nf+2)/2) * (W/nf + 0.29)' nrd='0.29 / W' nrs='0.29 / W'
+ sa=0 sb=0 sd=0 mult=1 m=1
XM74 ENN0 RST VSS VSS sky130_fd_pr__nfet_01v8 L=0.15 W=1 nf=1 ad='int((nf+1)/2) * W/nf * 0.29' as='int((nf+2)/2) * W/nf * 0.29'
+ pd='2*int((nf+1)/2) * (W/nf + 0.29)' ps='2*int((nf+2)/2) * (W/nf + 0.29)' nrd='0.29 / W' nrs='0.29 / W'
+ sa=0 sb=0 sd=0 mult=1 m=1
XM75 EN0 ENN0 VCC VCC sky130_fd_pr__pfet_01v8 L=0.15 W=2 nf=1 ad='int((nf+1)/2) * W/nf * 0.29' as='int((nf+2)/2) * W/nf * 0.29'
+ pd='2*int((nf+1)/2) * (W/nf + 0.29)' ps='2*int((nf+2)/2) * (W/nf + 0.29)' nrd='0.29 / W' nrs='0.29 / W'
+ sa=0 sb=0 sd=0 mult=1 m=1
XM76 EN0 ENN0 VSS VSS sky130_fd_pr__nfet_01v8 L=0.15 W=1 nf=1 ad='int((nf+1)/2) * W/nf * 0.29' as='int((nf+2)/2) * W/nf * 0.29'
+ pd='2*int((nf+1)/2) * (W/nf + 0.29)' ps='2*int((nf+2)/2) * (W/nf + 0.29)' nrd='0.29 / W' nrs='0.29 / W'
+ sa=0 sb=0 sd=0 mult=1 m=1
XM77 N1_0_p1 TRY0 VCC VCC sky130_fd_pr__pfet_01v8 L=0.15 W=4 nf=1 ad='int((nf+1)/2) * W/nf * 0.29' as='int((nf+2)/2) * W/nf * 0.29'
+ pd='2*int((nf+1)/2) * (W/nf + 0.29)' ps='2*int((nf+2)/2) * (W/nf + 0.29)' nrd='0.29 / W' nrs='0.29 / W'
+ sa=0 sb=0 sd=0 mult=1 m=1
XM78 N1_0 COML N1_0_p1 VCC sky130_fd_pr__pfet_01v8 L=0.15 W=4 nf=1 ad='int((nf+1)/2) * W/nf * 0.29' as='int((nf+2)/2) * W/nf * 0.29'
+ pd='2*int((nf+1)/2) * (W/nf + 0.29)' ps='2*int((nf+2)/2) * (W/nf + 0.29)' nrd='0.29 / W' nrs='0.29 / W'
+ sa=0 sb=0 sd=0 mult=1 m=1
XM79 N1_0 TRY0 VSS VSS sky130_fd_pr__nfet_01v8 L=0.15 W=1 nf=1 ad='int((nf+1)/2) * W/nf * 0.29' as='int((nf+2)/2) * W/nf * 0.29'
+ pd='2*int((nf+1)/2) * (W/nf + 0.29)' ps='2*int((nf+2)/2) * (W/nf + 0.29)' nrd='0.29 / W' nrs='0.29 / W'
+ sa=0 sb=0 sd=0 mult=1 m=1
XM80 N1_0 COML VSS VSS sky130_fd_pr__nfet_01v8 L=0.15 W=1 nf=1 ad='int((nf+1)/2) * W/nf * 0.29' as='int((nf+2)/2) * W/nf * 0.29'
+ pd='2*int((nf+1)/2) * (W/nf + 0.29)' ps='2*int((nf+2)/2) * (W/nf + 0.29)' nrd='0.29 / W' nrs='0.29 / W'
+ sa=0 sb=0 sd=0 mult=1 m=1
XM81 DIN0_p1 N1_0 VCC VCC sky130_fd_pr__pfet_01v8 L=0.15 W=4 nf=1 ad='int((nf+1)/2) * W/nf * 0.29' as='int((nf+2)/2) * W/nf * 0.29'
+ pd='2*int((nf+1)/2) * (W/nf + 0.29)' ps='2*int((nf+2)/2) * (W/nf + 0.29)' nrd='0.29 / W' nrs='0.29 / W'
+ sa=0 sb=0 sd=0 mult=1 m=1
XM82 DIN0 RST DIN0_p1 VCC sky130_fd_pr__pfet_01v8 L=0.15 W=4 nf=1 ad='int((nf+1)/2) * W/nf * 0.29' as='int((nf+2)/2) * W/nf * 0.29'
+ pd='2*int((nf+1)/2) * (W/nf + 0.29)' ps='2*int((nf+2)/2) * (W/nf + 0.29)' nrd='0.29 / W' nrs='0.29 / W'
+ sa=0 sb=0 sd=0 mult=1 m=1
XM83 DIN0 N1_0 VSS VSS sky130_fd_pr__nfet_01v8 L=0.15 W=1 nf=1 ad='int((nf+1)/2) * W/nf * 0.29' as='int((nf+2)/2) * W/nf * 0.29'
+ pd='2*int((nf+1)/2) * (W/nf + 0.29)' ps='2*int((nf+2)/2) * (W/nf + 0.29)' nrd='0.29 / W' nrs='0.29 / W'
+ sa=0 sb=0 sd=0 mult=1 m=1
XM84 DIN0 RST VSS VSS sky130_fd_pr__nfet_01v8 L=0.15 W=1 nf=1 ad='int((nf+1)/2) * W/nf * 0.29' as='int((nf+2)/2) * W/nf * 0.29'
+ pd='2*int((nf+1)/2) * (W/nf + 0.29)' ps='2*int((nf+2)/2) * (W/nf + 0.29)' nrd='0.29 / W' nrs='0.29 / W'
+ sa=0 sb=0 sd=0 mult=1 m=1
XM85 DIN0 EN0 X0 VSS sky130_fd_pr__nfet_01v8 L=0.15 W=1 nf=1 ad='int((nf+1)/2) * W/nf * 0.29' as='int((nf+2)/2) * W/nf * 0.29'
+ pd='2*int((nf+1)/2) * (W/nf + 0.29)' ps='2*int((nf+2)/2) * (W/nf + 0.29)' nrd='0.29 / W' nrs='0.29 / W'
+ sa=0 sb=0 sd=0 mult=1 m=1
XM86 X0 ENN0 DIN0 VCC sky130_fd_pr__pfet_01v8 L=0.15 W=2 nf=1 ad='int((nf+1)/2) * W/nf * 0.29' as='int((nf+2)/2) * W/nf * 0.29'
+ pd='2*int((nf+1)/2) * (W/nf + 0.29)' ps='2*int((nf+2)/2) * (W/nf + 0.29)' nrd='0.29 / W' nrs='0.29 / W'
+ sa=0 sb=0 sd=0 mult=1 m=1
XM87 B0N X0 VCC VCC sky130_fd_pr__pfet_01v8 L=0.15 W=2 nf=1 ad='int((nf+1)/2) * W/nf * 0.29' as='int((nf+2)/2) * W/nf * 0.29'
+ pd='2*int((nf+1)/2) * (W/nf + 0.29)' ps='2*int((nf+2)/2) * (W/nf + 0.29)' nrd='0.29 / W' nrs='0.29 / W'
+ sa=0 sb=0 sd=0 mult=1 m=1
XM88 B0N X0 VSS VSS sky130_fd_pr__nfet_01v8 L=0.15 W=1 nf=1 ad='int((nf+1)/2) * W/nf * 0.29' as='int((nf+2)/2) * W/nf * 0.29'
+ pd='2*int((nf+1)/2) * (W/nf + 0.29)' ps='2*int((nf+2)/2) * (W/nf + 0.29)' nrd='0.29 / W' nrs='0.29 / W'
+ sa=0 sb=0 sd=0 mult=1 m=1
XM89 D0 B0N VCC VCC sky130_fd_pr__pfet_01v8 L=0.15 W=2 nf=1 ad='int((nf+1)/2) * W/nf * 0.29' as='int((nf+2)/2) * W/nf * 0.29'
+ pd='2*int((nf+1)/2) * (W/nf + 0.29)' ps='2*int((nf+2)/2) * (W/nf + 0.29)' nrd='0.29 / W' nrs='0.29 / W'
+ sa=0 sb=0 sd=0 mult=1 m=1
XM90 D0 B0N VSS VSS sky130_fd_pr__nfet_01v8 L=0.15 W=1 nf=1 ad='int((nf+1)/2) * W/nf * 0.29' as='int((nf+2)/2) * W/nf * 0.29'
+ pd='2*int((nf+1)/2) * (W/nf + 0.29)' ps='2*int((nf+2)/2) * (W/nf + 0.29)' nrd='0.29 / W' nrs='0.29 / W'
+ sa=0 sb=0 sd=0 mult=1 m=1
XM91 D0 ENN0 X0 VSS sky130_fd_pr__nfet_01v8 L=0.15 W=1 nf=1 ad='int((nf+1)/2) * W/nf * 0.29' as='int((nf+2)/2) * W/nf * 0.29'
+ pd='2*int((nf+1)/2) * (W/nf + 0.29)' ps='2*int((nf+2)/2) * (W/nf + 0.29)' nrd='0.29 / W' nrs='0.29 / W'
+ sa=0 sb=0 sd=0 mult=1 m=1
XM92 X0 EN0 D0 VCC sky130_fd_pr__pfet_01v8 L=0.15 W=2 nf=1 ad='int((nf+1)/2) * W/nf * 0.29' as='int((nf+2)/2) * W/nf * 0.29'
+ pd='2*int((nf+1)/2) * (W/nf + 0.29)' ps='2*int((nf+2)/2) * (W/nf + 0.29)' nrd='0.29 / W' nrs='0.29 / W'
+ sa=0 sb=0 sd=0 mult=1 m=1
**.ends
.end
